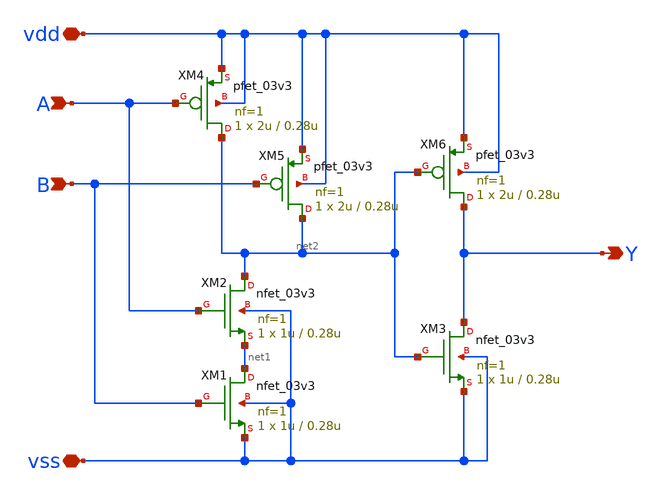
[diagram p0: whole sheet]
** sch_path: General/ADC/delay/and.sch
**.subckt and vdd vss A B Y
*.iopin vdd
*.iopin vss
*.ipin A
*.ipin B
*.opin Y
XM1 net1 B vss vss nfet_03v3 L=0.28u W=1u nf=1 ad='int((nf+1)/2) * W/nf * 0.18u' as='int((nf+2)/2) * W/nf * 0.18u'
+ pd='2*int((nf+1)/2) * (W/nf + 0.18u)' ps='2*int((nf+2)/2) * (W/nf + 0.18u)' nrd='0.18u / W' nrs='0.18u / W'
+ sa=0 sb=0 sd=0 m=1
XM2 net2 A net1 vss nfet_03v3 L=0.28u W=1u nf=1 ad='int((nf+1)/2) * W/nf * 0.18u' as='int((nf+2)/2) * W/nf * 0.18u'
+ pd='2*int((nf+1)/2) * (W/nf + 0.18u)' ps='2*int((nf+2)/2) * (W/nf + 0.18u)' nrd='0.18u / W' nrs='0.18u / W'
+ sa=0 sb=0 sd=0 m=1
XM3 Y net2 vss vss nfet_03v3 L=0.28u W=1u nf=1 ad='int((nf+1)/2) * W/nf * 0.18u' as='int((nf+2)/2) * W/nf * 0.18u'
+ pd='2*int((nf+1)/2) * (W/nf + 0.18u)' ps='2*int((nf+2)/2) * (W/nf + 0.18u)' nrd='0.18u / W' nrs='0.18u / W'
+ sa=0 sb=0 sd=0 m=1
XM4 net2 A vdd vdd pfet_03v3 L=0.28u W=2u nf=1 ad='int((nf+1)/2) * W/nf * 0.18u' as='int((nf+2)/2) * W/nf * 0.18u'
+ pd='2*int((nf+1)/2) * (W/nf + 0.18u)' ps='2*int((nf+2)/2) * (W/nf + 0.18u)' nrd='0.18u / W' nrs='0.18u / W'
+ sa=0 sb=0 sd=0 m=1
XM5 net2 B vdd vdd pfet_03v3 L=0.28u W=2u nf=1 ad='int((nf+1)/2) * W/nf * 0.18u' as='int((nf+2)/2) * W/nf * 0.18u'
+ pd='2*int((nf+1)/2) * (W/nf + 0.18u)' ps='2*int((nf+2)/2) * (W/nf + 0.18u)' nrd='0.18u / W' nrs='0.18u / W'
+ sa=0 sb=0 sd=0 m=1
XM6 Y net2 vdd vdd pfet_03v3 L=0.28u W=2u nf=1 ad='int((nf+1)/2) * W/nf * 0.18u' as='int((nf+2)/2) * W/nf * 0.18u'
+ pd='2*int((nf+1)/2) * (W/nf + 0.18u)' ps='2*int((nf+2)/2) * (W/nf + 0.18u)' nrd='0.18u / W' nrs='0.18u / W'
+ sa=0 sb=0 sd=0 m=1
**.ends
.end
